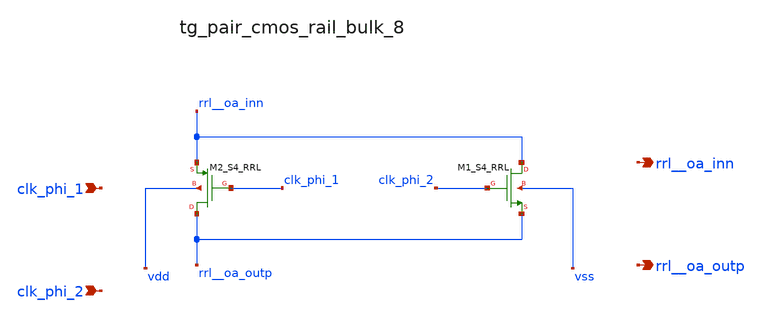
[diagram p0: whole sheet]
** sch_path: analog-db/raw/ia_004_fan_chopper_rrl/hier/blocks/tg_pair_cmos_rail_bulk_8.sch
**.subckt tg_pair_cmos_rail_bulk_8 clk_phi_1 clk_phi_2 rrl__oa_inn rrl__oa_outp
*.ipin clk_phi_1
*.ipin clk_phi_2
*.opin rrl__oa_inn
*.opin rrl__oa_outp
XM1_S4_RRL rrl__oa_inn clk_phi_2 rrl__oa_outp vss sg13_lv_nmos w=x_dut_xm1_s4_rrl_w
+ l=x_dut_xm1_s4_rrl_l ng=1 m=x_dut_xm1_s4_rrl_m
XM2_S4_RRL rrl__oa_outp clk_phi_1 rrl__oa_inn vdd sg13_lv_pmos w=x_dut_xm2_s4_rrl_w
+ l=x_dut_xm2_s4_rrl_l ng=1 m=x_dut_xm2_s4_rrl_m
**.ends
.end
